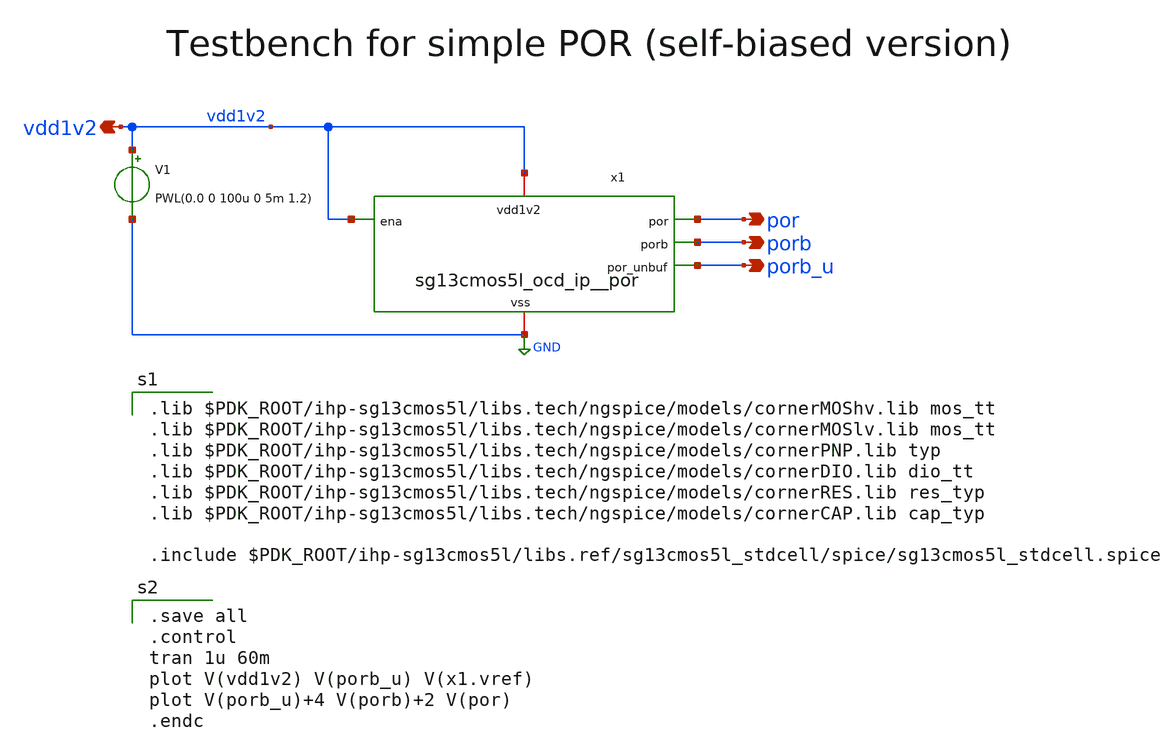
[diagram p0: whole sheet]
** sch_path: xschem/por_unregulated_tb.sch
**.subckt por_unregulated_tb vdd1v2 porb_u porb por
*.opin vdd1v2
*.opin porb_u
*.opin porb
*.opin por
V1 vdd1v2 GND PWL(0.0 0 100u 0 5m 1.2)
x1 vdd1v2 vdd1v2 porb_u GND porb por sg13cmos5l_ocd_ip__por
**** begin user architecture code

.save all
.control
tran 1u 60m
plot V(vdd1v2) V(porb_u) V(x1.vref)
plot V(porb_u)+4 V(porb)+2 V(por)
.endc


.lib $PDK_ROOT/ihp-sg13cmos5l/libs.tech/ngspice/models/cornerMOShv.lib mos_tt
.lib $PDK_ROOT/ihp-sg13cmos5l/libs.tech/ngspice/models/cornerMOSlv.lib mos_tt
.lib $PDK_ROOT/ihp-sg13cmos5l/libs.tech/ngspice/models/cornerPNP.lib typ
.lib $PDK_ROOT/ihp-sg13cmos5l/libs.tech/ngspice/models/cornerDIO.lib dio_tt
.lib $PDK_ROOT/ihp-sg13cmos5l/libs.tech/ngspice/models/cornerRES.lib res_typ
.lib $PDK_ROOT/ihp-sg13cmos5l/libs.tech/ngspice/models/cornerCAP.lib cap_typ

.include $PDK_ROOT/ihp-sg13cmos5l/libs.ref/sg13cmos5l_stdcell/spice/sg13cmos5l_stdcell.spice

**** end user architecture code
**.ends

* expanding   symbol:  sg13cmos5l_ocd_ip__por.sym # of pins=6
** sym_path: xschem/sg13cmos5l_ocd_ip__por.sym
** sch_path: xschem/sg13cmos5l_ocd_ip__por.sch
.subckt sg13cmos5l_ocd_ip__por vdd1v2 ena por_unbuf vss porb por
*.ipin ena
*.iopin vdd1v2
*.iopin vss
*.opin por_unbuf
*.opin porb
*.opin por
x1 vdd1v2 vpb vref vfb ena vss net2 por_amp
x2 vdd1v2 vcap por_unbuf vss por_1v2_schmitt_inv
x7 vdd1v2 vss sg13cmos5l_decap_4
x5 por por_unbuf vdd1v2 vss sg13cmos5l_buf_16
x6 net1 por_unbuf vdd1v2 vss sg13cmos5l_inv_4
x3 porb net1 vdd1v2 vss sg13cmos5l_buf_16
XR3 vdd1v2 vref vss rhigh w=0.5e-6 l=908.28e-6 m=1 b=0 mm_ok=1
XR1 vfb vss vss rhigh w=0.5e-6 l=908.28e-6 m=1 b=0 mm_ok=1
XC2 vref vpb cap_cmomf w=50e-6 l=14e-6 mmin=3 mmax=4 subblock=0 rfmodel=0 subscale=1 m=1 mm_ok=1
XC1 vcap vss cap_cmomf w=20e-6 l=20e-6 mmin=1 mmax=4 subblock=0 rfmodel=0 subscale=1 m=16 mm_ok=1
XD2 vss ena dantenna l=0.78u w=0.78u
XC3 vdd1v2 vss cap_cmomf w=50e-6 l=14e-6 mmin=3 mmax=4 subblock=0 rfmodel=0 subscale=1 m=1 mm_ok=1
XC4 vcap vss cap_cmomf w=50e-6 l=14e-6 mmin=1 mmax=4 subblock=1 rfmodel=0 subscale=1 m=2 mm_ok=1
x4 vdd1v2 vref vpb vcap vfb net2 vss por_stepdown
.ends


* expanding   symbol:  por_amp.sym # of pins=7
** sym_path: xschem/por_amp.sym
** sch_path: xschem/por_amp.sch
.subckt por_amp vdd1v2 out inn inp ena vss nbias
*.ipin ena
*.ipin inp
*.ipin inn
*.opin out
*.iopin vdd1v2
*.iopin vss
*.ipin nbias
XM10 vdd1v2 vdd1v2 vdd1v2 vdd1v2 sg13_lv_pmos w=1.88u l=0.13u ng=4 m=1 mm_ok=1
XM11 vss vss vss vss sg13_lv_nmos w=0.94u l=0.13u ng=2 m=1 mm_ok=1
XM8 nc vss vss vss sg13_lv_nmos w=0.94u l=0.13u ng=2 m=1 mm_ok=1
XM1 out net1 vdd1v2 vdd1v2 sg13_lv_pmos w=2.82u l=0.13u ng=6 m=1 mm_ok=1
XM2 net1 net1 vdd1v2 vdd1v2 sg13_lv_pmos w=2.82u l=0.13u ng=6 m=1 mm_ok=1
XM3 net2 nbias vss vss sg13_lv_nmos w=5.64u l=0.13u ng=12 m=1 mm_ok=1
XM4 nc ena net2 vss sg13_lv_nmos w=5.64u l=0.13u ng=12 m=1 mm_ok=1
XM5 net1 inp nc vss sg13_lv_nmos w=5.64u l=0.13u ng=12 m=1 mm_ok=1
XM6 out inn nc vss sg13_lv_nmos w=5.64u l=0.13u ng=12 m=1 mm_ok=1
.ends


* expanding   symbol:  por_1v2_schmitt_inv.sym # of pins=4
** sym_path: xschem/por_1v2_schmitt_inv.sym
** sch_path: xschem/por_1v2_schmitt_inv.sch
.subckt por_1v2_schmitt_inv vdd1v2 in out vss
*.iopin vdd1v2
*.iopin vss
*.ipin in
*.opin out
XM7 out in n1 vss sg13_lv_nmos w=0.7u l=0.13u ng=2 m=1 mm_ok=1
XM8 p1 in vdd1v2 vdd1v2 sg13_lv_pmos w=1.4u l=0.13u ng=4 m=1 mm_ok=1
XM2 out in p1 vdd1v2 sg13_lv_pmos w=0.35u l=0.13u ng=1 m=1 mm_ok=1
XM3 vss out p1 vdd1v2 sg13_lv_pmos w=1.4u l=0.26u ng=1 m=1 mm_ok=1
XM1 n1 in vss vss sg13_lv_nmos w=0.7u l=0.13u ng=2 m=1 mm_ok=1
XM4 vdd1v2 out n1 vss sg13_lv_nmos w=2.8u l=0.26u ng=1 m=1 mm_ok=1
.ends


* expanding   symbol:  por_stepdown.sym # of pins=7
** sym_path: xschem/por_stepdown.sym
** sch_path: xschem/por_stepdown.sch
.subckt por_stepdown vdd1v2 vref vpb vcap vfb nbias vss
*.iopin vdd1v2
*.iopin vss
*.opin nbias
*.ipin vref
*.ipin vpb
*.opin vfb
*.opin vcap
Vmeas vdd1v2 net7 0
.save i(vmeas)
Vmeas1 vdd1v2 net6 0
.save i(vmeas1)
Vmeas2 vdd1v2 net5 0
.save i(vmeas2)
Vmeas3 vdd1v2 net4 0
.save i(vmeas3)
Vmeas4 vref net8 0
.save i(vmeas4)
XM26 net1 vpb net7 vdd1v2 sg13_lv_pmos w=2.88u l=0.13u ng=12 m=1 mm_ok=1
XM27 net8 net8 nbias vss sg13_lv_nmos w=3.76u l=0.13u ng=8 m=1 mm_ok=1
XM13 nbias nbias vss vss sg13_lv_nmos w=3.76u l=0.13u ng=8 m=1 mm_ok=1
XM1 nb1 nb1 net2 vss sg13_lv_nmos w=2.88u l=0.13u ng=12 m=1 mm_ok=1
XM6 net2 net2 vss vss sg13_lv_nmos w=2.88u l=0.13u ng=12 m=1 mm_ok=1
XM7 n1 net2 vss vss sg13_lv_nmos w=0.24u l=0.13u ng=1 m=1 mm_ok=1
XM8 pb1 nb1 n1 vss sg13_lv_nmos w=0.24u l=0.13u ng=1 m=1 mm_ok=1
XM14 vss vss vss vss sg13_lv_nmos w=0.24u l=0.13u ng=1 m=1 mm_ok=1
XM19 n1 vss vss vss sg13_lv_nmos w=0.24u l=0.13u ng=1 m=1 mm_ok=1
XM20 n1 vss nb1 vss sg13_lv_nmos w=0.24u l=0.13u ng=1 m=1 mm_ok=1
XM21 nb1 vss vss vss sg13_lv_nmos w=0.24u l=0.13u ng=1 m=1 mm_ok=1
XM15 vdd1v2 vdd1v2 vdd1v2 vdd1v2 sg13_lv_pmos w=0.24u l=0.13u ng=1 m=2 mm_ok=1
XM16 vdd1v2 vdd1v2 p1 vdd1v2 sg13_lv_pmos w=0.24u l=0.13u ng=1 m=1 mm_ok=1
XM17 vfb vdd1v2 p1 vdd1v2 sg13_lv_pmos w=0.24u l=0.13u ng=1 m=1 mm_ok=1
XM18 vdd1v2 vdd1v2 vfb vdd1v2 sg13_lv_pmos w=0.24u l=0.13u ng=1 m=1 mm_ok=1
XM22 vdd1v2 vdd1v2 p2 vdd1v2 sg13_lv_pmos w=0.24u l=0.13u ng=1 m=1 mm_ok=1
XM23 pb1 vdd1v2 p2 vdd1v2 sg13_lv_pmos w=0.24u l=0.13u ng=1 m=1 mm_ok=1
XM24 vdd1v2 vdd1v2 pb1 vdd1v2 sg13_lv_pmos w=0.24u l=0.13u ng=1 m=1 mm_ok=1
XM2 vfb vfb net1 vdd1v2 sg13_lv_pmos w=2.88u l=0.13u ng=12 m=1 mm_ok=1
XM3 p2 net3 net4 vdd1v2 sg13_lv_pmos w=0.24u l=0.13u ng=1 m=1 mm_ok=1
XM4 vcap pb1 p2 vdd1v2 sg13_lv_pmos w=0.24u l=0.13u ng=1 m=1 mm_ok=1
XM5 p1 vpb net6 vdd1v2 sg13_lv_pmos w=0.24u l=0.13u ng=1 m=1 mm_ok=1
XM9 nb1 vfb p1 vdd1v2 sg13_lv_pmos w=0.24u l=0.13u ng=1 m=1 mm_ok=1
XM10 net3 net3 net5 vdd1v2 sg13_lv_pmos w=1.92u l=0.13u ng=8 m=1 mm_ok=1
XM11 pb1 pb1 net3 vdd1v2 sg13_lv_pmos w=1.92u l=0.13u ng=8 m=1 mm_ok=1
.ends

.GLOBAL GND
.end
